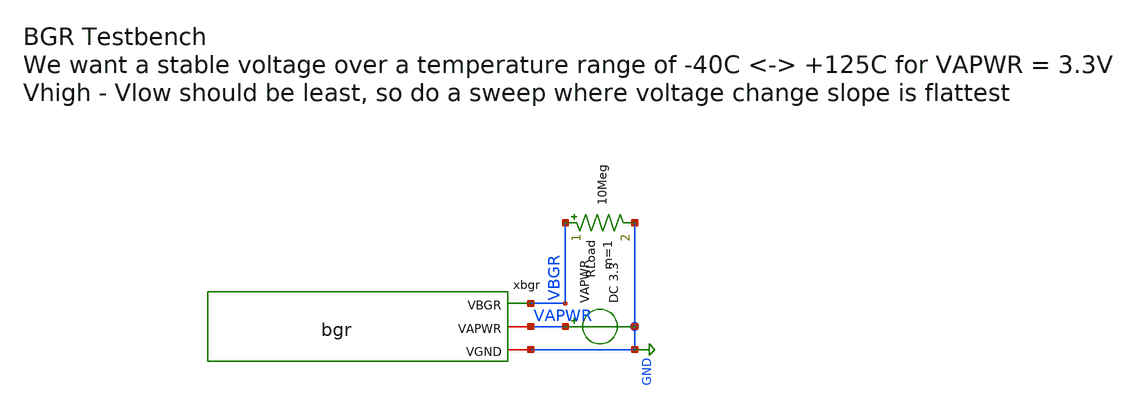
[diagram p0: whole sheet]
** sch_path: xschem/tb_bgr.sch
**.subckt tb_bgr
VAPWR VAPWR GND DC 3.3
xbgr VBGR VAPWR GND bgr
RLoad VBGR GND 10Meg m=1
**** begin user architecture code


.param sw_stat_global=1  ; enable statistical variation (0 = OFF, 1 = ON)
.param mc_skew=1         ; MOS variation scale factor (1 = Nominal)
.param res_mc_skew=1     ; resistor variation scale factor (1 = Nominal)
.param fnoicor=0         ; flicker noise model selector
.param sw_stat_mismatch=0
.lib /foss/pdks/gf180mcuD/libs.tech/ngspice/sm141064.ngspice statistical
.lib /foss/pdks/gf180mcuD/libs.tech/ngspice/sm141064.ngspice bjt_statistical
.lib /foss/pdks/gf180mcuD/libs.tech/ngspice/sm141064.ngspice res_statistical
.control
  dc TEMP -40 125 5
  display
  plot v(VBGR)
  plot v(xbgr.xbgr_core.E2)-v(xbgr.xbgr_core.E1)
  plot v(xbgr.xbgr_core.BIAS_P)
  plot v(xbgr.xbgr_core.E1)
.endc


**** end user architecture code
**.ends

* expanding   symbol:  bgr.sym # of pins=3
** sym_path: xschem/bgr.sym
** sch_path: xschem/bgr.sch
.subckt bgr VBGR VAPWR VGND
*.iopin VAPWR
*.iopin VGND
*.opin VBGR
xbgr_core net4 VAPWR net3 net1 net2 VBGR VGND bgr_core_without_amp
xbgr_amp net4 VAPWR net1 net2 net3 VGND bgr_error_amp
xbgr_startup VAPWR VBGR net4 net3 VGND bgr_startup
.ends


* expanding   symbol:  bgr_core_without_amp.sym # of pins=7
** sym_path: xschem/bgr_core_without_amp.sym
** sch_path: xschem/bgr_core_without_amp.sch
.subckt bgr_core_without_amp BIAS_P VAPWR VCTRL VN2 VN1 VBGR VGND
*.iopin VGND
*.iopin VAPWR
*.opin VBGR
*.ipin VCTRL
*.opin BIAS_P
*.opin VN1
*.opin VN2
XQ1 VN1 VBGR E1 VGND npn_05p00x05p00 m=1
XQ2 VN2 VBGR E2 VGND npn_05p00x05p00 m=8
XR1 E1 E2 VGND ppolyf_u_1k r_width=1.18e-6 r_length=3e-6 m=1
XR2 VGND E1 VGND ppolyf_u_1k r_width=1e-6 r_length=62.65e-6 m=1
XR3 VGND VBGR VGND ppolyf_u_1k r_width=1e-6 r_length=137e-6 m=1
XM1 VN2 VCTRL VAPWR VAPWR pfet_03v3 L=4u W=8u nf=1 ad='int((nf+1)/2) * W/nf * 0.18u' as='int((nf+2)/2) * W/nf * 0.18u'
+ pd='2*int((nf+1)/2) * (W/nf + 0.18u)' ps='2*int((nf+2)/2) * (W/nf + 0.18u)' nrd='0.18u / W' nrs='0.18u / W'
+ sa=0 sb=0 sd=0 m=1
XM2 VN1 VCTRL VAPWR VAPWR pfet_03v3 L=4u W=8u nf=1 ad='int((nf+1)/2) * W/nf * 0.18u' as='int((nf+2)/2) * W/nf * 0.18u'
+ pd='2*int((nf+1)/2) * (W/nf + 0.18u)' ps='2*int((nf+2)/2) * (W/nf + 0.18u)' nrd='0.18u / W' nrs='0.18u / W'
+ sa=0 sb=0 sd=0 m=1
XM3 NBIAS_N VCTRL VAPWR VAPWR pfet_03v3 L=4u W=2u nf=1 ad='int((nf+1)/2) * W/nf * 0.18u' as='int((nf+2)/2) * W/nf * 0.18u'
+ pd='2*int((nf+1)/2) * (W/nf + 0.18u)' ps='2*int((nf+2)/2) * (W/nf + 0.18u)' nrd='0.18u / W' nrs='0.18u / W'
+ sa=0 sb=0 sd=0 m=1
XM4 VBGR VCTRL VAPWR VAPWR pfet_03v3 L=4u W=64u nf=1 ad='int((nf+1)/2) * W/nf * 0.18u' as='int((nf+2)/2) * W/nf * 0.18u'
+ pd='2*int((nf+1)/2) * (W/nf + 0.18u)' ps='2*int((nf+2)/2) * (W/nf + 0.18u)' nrd='0.18u / W' nrs='0.18u / W'
+ sa=0 sb=0 sd=0 m=1
XM5 BIAS_P BIAS_P VAPWR VAPWR pfet_03v3 L=4u W=1u nf=1 ad='int((nf+1)/2) * W/nf * 0.18u' as='int((nf+2)/2) * W/nf * 0.18u'
+ pd='2*int((nf+1)/2) * (W/nf + 0.18u)' ps='2*int((nf+2)/2) * (W/nf + 0.18u)' nrd='0.18u / W' nrs='0.18u / W'
+ sa=0 sb=0 sd=0 m=1
XM6 BIAS_P NBIAS_N VGND VGND nfet_03v3 L=4u W=1u nf=1 ad='int((nf+1)/2) * W/nf * 0.18u' as='int((nf+2)/2) * W/nf * 0.18u'
+ pd='2*int((nf+1)/2) * (W/nf + 0.18u)' ps='2*int((nf+2)/2) * (W/nf + 0.18u)' nrd='0.18u / W' nrs='0.18u / W'
+ sa=0 sb=0 sd=0 m=1
XM7 NBIAS_N NBIAS_N VGND VGND nfet_03v3 L=4u W=1u nf=1 ad='int((nf+1)/2) * W/nf * 0.18u' as='int((nf+2)/2) * W/nf * 0.18u'
+ pd='2*int((nf+1)/2) * (W/nf + 0.18u)' ps='2*int((nf+2)/2) * (W/nf + 0.18u)' nrd='0.18u / W' nrs='0.18u / W'
+ sa=0 sb=0 sd=0 m=1
.ends


* expanding   symbol:  bgr_error_amp.sym # of pins=6
** sym_path: xschem/bgr_error_amp.sym
** sch_path: xschem/bgr_error_amp.sch
.subckt bgr_error_amp BIAS_P VAPWR VIN_P VIN_N VOUT VGND
*.ipin VIN_P
*.ipin VIN_N
*.ipin BIAS_P
*.iopin VAPWR
*.iopin VGND
*.opin VOUT
XMDIFF_P net1 VIN_P TAIL_P VAPWR pfet_03v3 L=0.28u W=0.22u nf=1 ad='int((nf+1)/2) * W/nf * 0.18u' as='int((nf+2)/2) * W/nf * 0.18u'
+ pd='2*int((nf+1)/2) * (W/nf + 0.18u)' ps='2*int((nf+2)/2) * (W/nf + 0.18u)' nrd='0.18u / W' nrs='0.18u / W'
+ sa=0 sb=0 sd=0 m=1
XMDIFF_N VOUT VIN_N TAIL_P VAPWR pfet_03v3 L=0.28u W=0.22u nf=1 ad='int((nf+1)/2) * W/nf * 0.18u' as='int((nf+2)/2) * W/nf * 0.18u'
+ pd='2*int((nf+1)/2) * (W/nf + 0.18u)' ps='2*int((nf+2)/2) * (W/nf + 0.18u)' nrd='0.18u / W' nrs='0.18u / W'
+ sa=0 sb=0 sd=0 m=1
XMTAIL TAIL_P BIAS_P VAPWR VAPWR pfet_03v3 L=0.28u W=0.22u nf=1 ad='int((nf+1)/2) * W/nf * 0.18u' as='int((nf+2)/2) * W/nf * 0.18u'
+ pd='2*int((nf+1)/2) * (W/nf + 0.18u)' ps='2*int((nf+2)/2) * (W/nf + 0.18u)' nrd='0.18u / W' nrs='0.18u / W'
+ sa=0 sb=0 sd=0 m=1
XMLOAD_REF net1 net1 VGND VGND nfet_03v3 L=0.28u W=0.22u nf=1 ad='int((nf+1)/2) * W/nf * 0.18u' as='int((nf+2)/2) * W/nf * 0.18u'
+ pd='2*int((nf+1)/2) * (W/nf + 0.18u)' ps='2*int((nf+2)/2) * (W/nf + 0.18u)' nrd='0.18u / W' nrs='0.18u / W'
+ sa=0 sb=0 sd=0 m=1
XMLOAD_OUT VOUT net1 VGND VGND nfet_03v3 L=0.28u W=0.22u nf=1 ad='int((nf+1)/2) * W/nf * 0.18u' as='int((nf+2)/2) * W/nf * 0.18u'
+ pd='2*int((nf+1)/2) * (W/nf + 0.18u)' ps='2*int((nf+2)/2) * (W/nf + 0.18u)' nrd='0.18u / W' nrs='0.18u / W'
+ sa=0 sb=0 sd=0 m=1
.ends


* expanding   symbol:  bgr_startup.sym # of pins=5
** sym_path: xschem/bgr_startup.sym
** sch_path: xschem/bgr_startup.sch
.subckt bgr_startup VAPWR VBGR BIAS_P VCTRL VGND
*.iopin VAPWR
*.iopin VGND
*.ipin VBGR
*.iopin BIAS_P
*.iopin VCTRL
XM1 START_ON VBGR VGND VGND nfet_03v3 L=0.28u W=0.22u nf=1 ad='int((nf+1)/2) * W/nf * 0.18u' as='int((nf+2)/2) * W/nf * 0.18u'
+ pd='2*int((nf+1)/2) * (W/nf + 0.18u)' ps='2*int((nf+2)/2) * (W/nf + 0.18u)' nrd='0.18u / W' nrs='0.18u / W'
+ sa=0 sb=0 sd=0 m=1
XM2 BIAS_P START_ON VGND VGND nfet_03v3 L=0.28u W=0.22u nf=1 ad='int((nf+1)/2) * W/nf * 0.18u' as='int((nf+2)/2) * W/nf * 0.18u'
+ pd='2*int((nf+1)/2) * (W/nf + 0.18u)' ps='2*int((nf+2)/2) * (W/nf + 0.18u)' nrd='0.18u / W' nrs='0.18u / W'
+ sa=0 sb=0 sd=0 m=1
XM3 VCTRL START_ON VGND VGND nfet_03v3 L=0.28u W=0.22u nf=1 ad='int((nf+1)/2) * W/nf * 0.18u' as='int((nf+2)/2) * W/nf * 0.18u'
+ pd='2*int((nf+1)/2) * (W/nf + 0.18u)' ps='2*int((nf+2)/2) * (W/nf + 0.18u)' nrd='0.18u / W' nrs='0.18u / W'
+ sa=0 sb=0 sd=0 m=1
XM4 START_ON VBGR VAPWR VAPWR pfet_03v3 L=0.28u W=0.22u nf=1 ad='int((nf+1)/2) * W/nf * 0.18u' as='int((nf+2)/2) * W/nf * 0.18u'
+ pd='2*int((nf+1)/2) * (W/nf + 0.18u)' ps='2*int((nf+2)/2) * (W/nf + 0.18u)' nrd='0.18u / W' nrs='0.18u / W'
+ sa=0 sb=0 sd=0 m=1
.ends

.GLOBAL GND
.end
